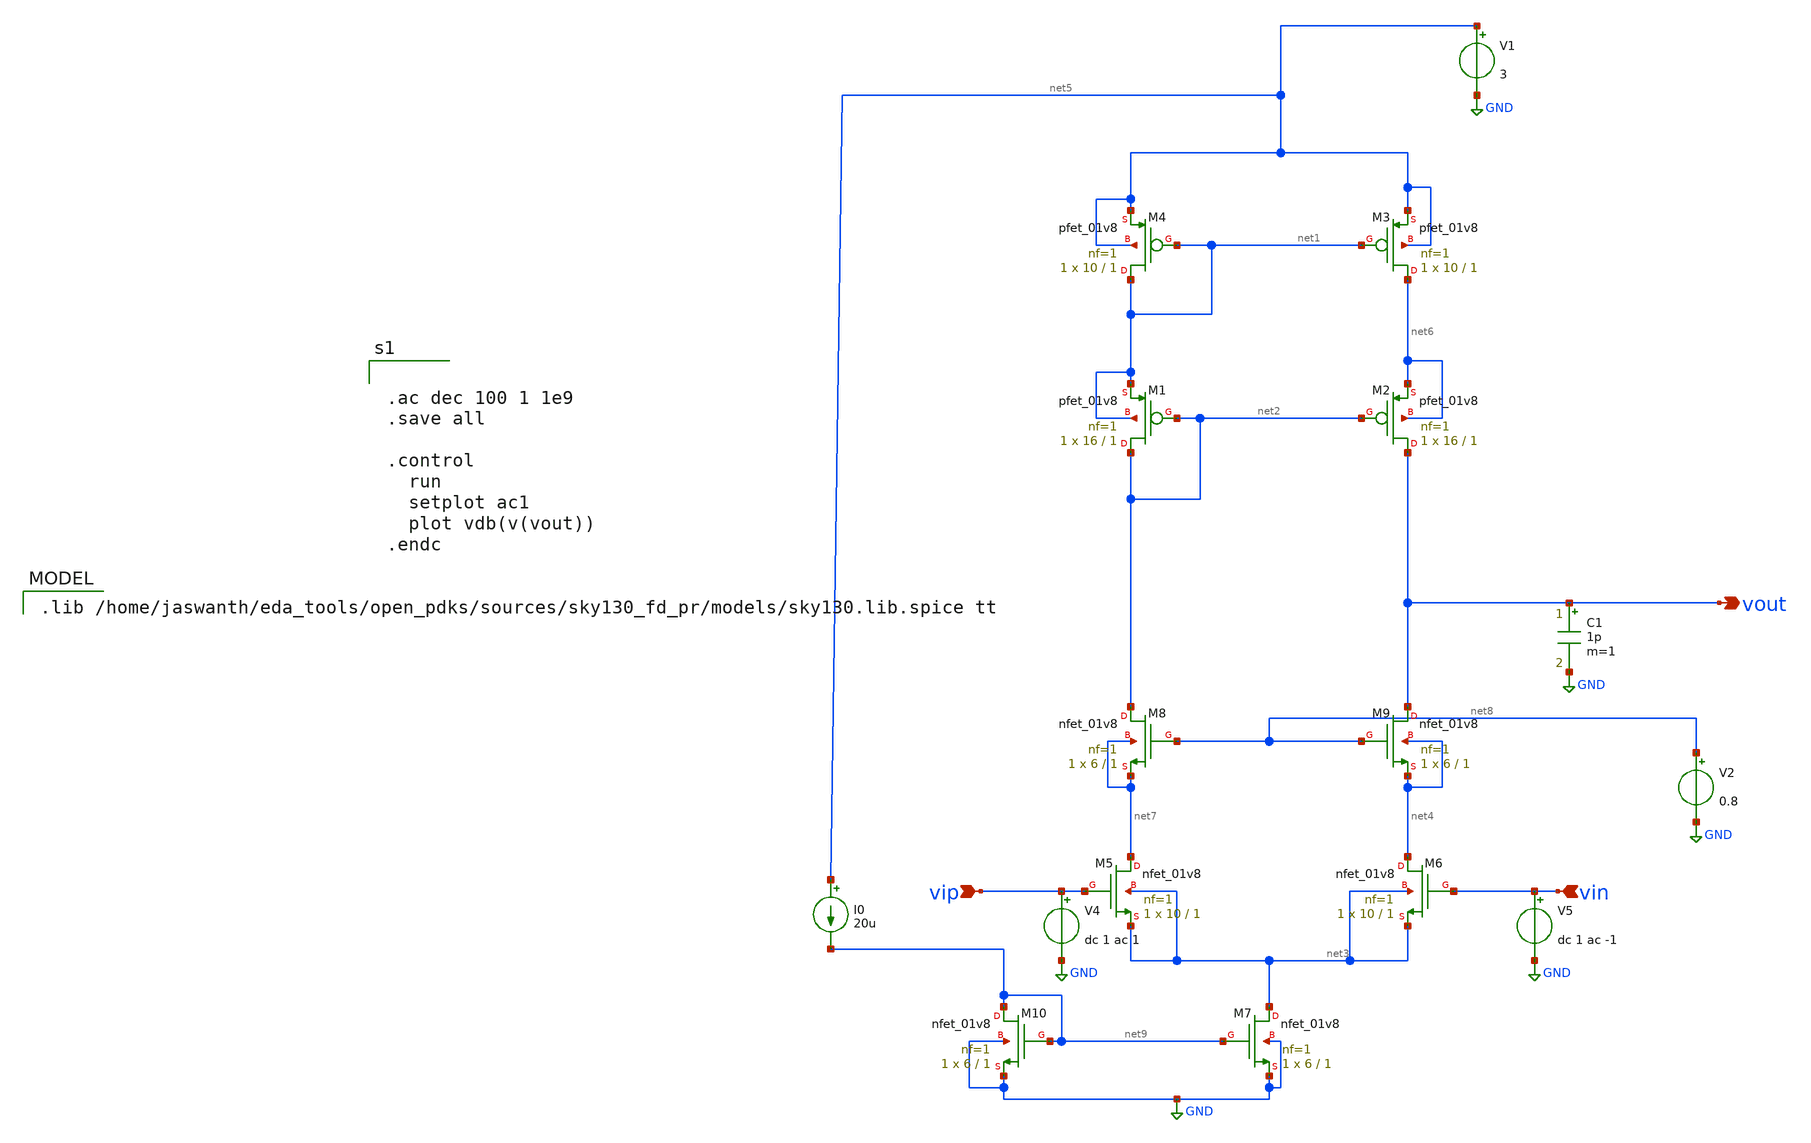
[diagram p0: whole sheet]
** sch_path: Telescopic_opamp/new_9t.sch
**.subckt new_9t vout vip vin
*.opin vout
*.ipin vip
*.ipin vin
XM3 net6 net1 net5 net5 sky130_fd_pr__pfet_01v8 L=1 W=10 nf=1 ad='int((1 + 1)/2) * 10 / 1 * 0.29' as='int((1 + 2)/2) * 10 / 1 * 0.29'
+ pd='2*int((1 + 1)/2) * (10 / 1 + 0.29)' ps='2*int((1 + 2)/2) * (10 / 1 + 0.29)' nrd='0.29 / 10 ' nrs='0.29 / 10 '
+ sa=0 sb=0 sd=0 mult=1 m=1
XM4 net1 net1 net5 net5 sky130_fd_pr__pfet_01v8 L=1 W=10 nf=1 ad='int((1 + 1)/2) * 10 / 1 * 0.29' as='int((1 + 2)/2) * 10 / 1 * 0.29'
+ pd='2*int((1 + 1)/2) * (10 / 1 + 0.29)' ps='2*int((1 + 2)/2) * (10 / 1 + 0.29)' nrd='0.29 / 10 ' nrs='0.29 / 10 '
+ sa=0 sb=0 sd=0 mult=1 m=1
XM5 net7 vip net3 net3 sky130_fd_pr__nfet_01v8 L=1 W=10 nf=1 ad='int((1 + 1)/2) * 10 / 1 * 0.29' as='int((1 + 2)/2) * 10 / 1 * 0.29'
+ pd='2*int((1 + 1)/2) * (10 / 1 + 0.29)' ps='2*int((1 + 2)/2) * (10 / 1 + 0.29)' nrd='0.29 / 10 ' nrs='0.29 / 10 '
+ sa=0 sb=0 sd=0 mult=1 m=1
XM6 net4 vin net3 net3 sky130_fd_pr__nfet_01v8 L=1 W=10 nf=1 ad='int((1 + 1)/2) * 10 / 1 * 0.29' as='int((1 + 2)/2) * 10 / 1 * 0.29'
+ pd='2*int((1 + 1)/2) * (10 / 1 + 0.29)' ps='2*int((1 + 2)/2) * (10 / 1 + 0.29)' nrd='0.29 / 10 ' nrs='0.29 / 10 '
+ sa=0 sb=0 sd=0 mult=1 m=1
XM7 net3 net9 GND GND sky130_fd_pr__nfet_01v8 L=1 W=6 nf=1 ad='int((1 + 1)/2) * 6 / 1 * 0.29' as='int((1 + 2)/2) * 6 / 1 * 0.29'
+ pd='2*int((1 + 1)/2) * (6 / 1 + 0.29)' ps='2*int((1 + 2)/2) * (6 / 1 + 0.29)' nrd='0.29 / 6 ' nrs='0.29 / 6 '
+ sa=0 sb=0 sd=0 mult=1 m=1
XM1 net2 net2 net1 net1 sky130_fd_pr__pfet_01v8 L=1 W=16 nf=1 ad='int((1 + 1)/2) * 16 / 1 * 0.29' as='int((1 + 2)/2) * 16 / 1 * 0.29'
+ pd='2*int((1 + 1)/2) * (16 / 1 + 0.29)' ps='2*int((1 + 2)/2) * (16 / 1 + 0.29)' nrd='0.29 / 16 ' nrs='0.29 / 16 '
+ sa=0 sb=0 sd=0 mult=1 m=1
XM2 vout net2 net6 net6 sky130_fd_pr__pfet_01v8 L=1 W=16 nf=1 ad='int((1 + 1)/2) * 16 / 1 * 0.29' as='int((1 + 2)/2) * 16 / 1 * 0.29'
+ pd='2*int((1 + 1)/2) * (16 / 1 + 0.29)' ps='2*int((1 + 2)/2) * (16 / 1 + 0.29)' nrd='0.29 / 16 ' nrs='0.29 / 16 '
+ sa=0 sb=0 sd=0 mult=1 m=1
XM8 net2 net8 net7 net7 sky130_fd_pr__nfet_01v8 L=1 W=6 nf=1 ad='int((1 + 1)/2) * 6 / 1 * 0.29' as='int((1 + 2)/2) * 6 / 1 * 0.29'
+ pd='2*int((1 + 1)/2) * (6 / 1 + 0.29)' ps='2*int((1 + 2)/2) * (6 / 1 + 0.29)' nrd='0.29 / 6 ' nrs='0.29 / 6 '
+ sa=0 sb=0 sd=0 mult=1 m=1
XM9 vout net8 net4 net4 sky130_fd_pr__nfet_01v8 L=1 W=6 nf=1 ad='int((1 + 1)/2) * 6 / 1 * 0.29' as='int((1 + 2)/2) * 6 / 1 * 0.29'
+ pd='2*int((1 + 1)/2) * (6 / 1 + 0.29)' ps='2*int((1 + 2)/2) * (6 / 1 + 0.29)' nrd='0.29 / 6 ' nrs='0.29 / 6 '
+ sa=0 sb=0 sd=0 mult=1 m=1
V1 net5 GND 3
C1 vout GND 1p m=1
V2 net8 GND 0.8
V4 vip GND dc 1 ac 1
V5 vin GND dc 1 ac -1
XM10 net9 net9 GND GND sky130_fd_pr__nfet_01v8 L=1 W=6 nf=1 ad='int((1 + 1)/2) * 6 / 1 * 0.29' as='int((1 + 2)/2) * 6 / 1 * 0.29'
+ pd='2*int((1 + 1)/2) * (6 / 1 + 0.29)' ps='2*int((1 + 2)/2) * (6 / 1 + 0.29)' nrd='0.29 / 6 ' nrs='0.29 / 6 '
+ sa=0 sb=0 sd=0 mult=1 m=1
I0 net5 net9 20u
**** begin user architecture code


.ac dec 100 1 1e9
.save all

.control
  run
  setplot ac1
  plot vdb(v(vout))
.endc


.lib /home/jaswanth/eda_tools/open_pdks/sources/sky130_fd_pr/models/sky130.lib.spice tt

**** end user architecture code
**.ends
.GLOBAL GND
.end
